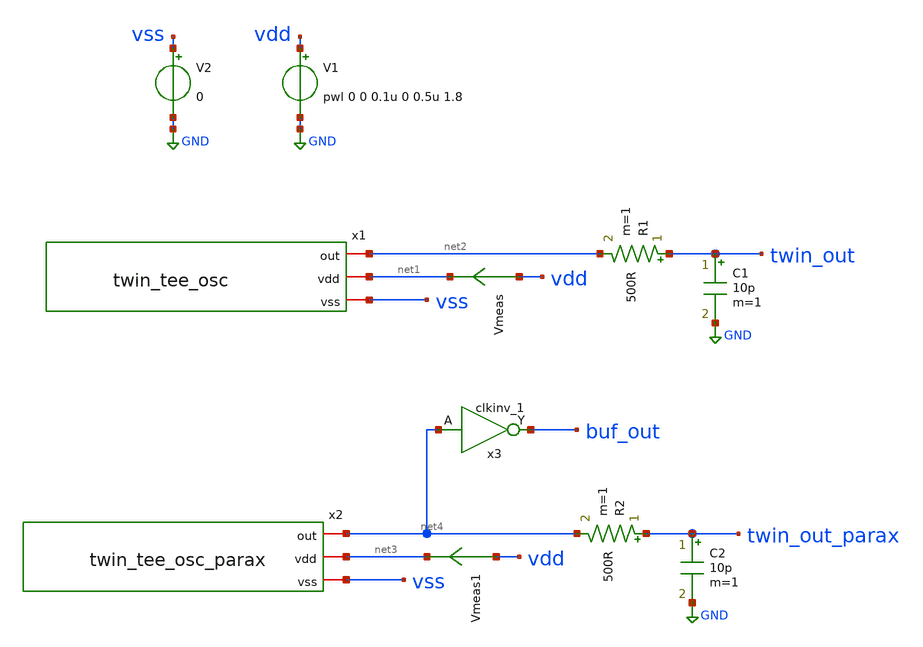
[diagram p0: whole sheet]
** sch_path: xschem/tb_twin_tee_osc.sch
**.subckt tb_twin_tee_osc
V1 vdd GND pwl 0 0 0.1u 0 0.5u 1.8
V2 vss GND 0
x1 net2 net1 vss twin_tee_osc
Vmeas vdd net1 0
R1 twin_out net2 500R m=1
C1 twin_out GND 10p m=1
x2 net4 net3 vss twin_tee_osc_parax
Vmeas1 vdd net3 0
R2 twin_out_parax net4 500R m=1
C2 twin_out_parax GND 10p m=1
x3 net4 vss vss vdd vdd buf_out sky130_fd_sc_hd__clkinv_1
**** begin user architecture code

** opencircuitdesign pdks install
.lib $::SKYWATER_MODELS/sky130.lib.spice tt_mm
.include $::SKYWATER_STDCELLS/sky130_fd_sc_hd.spice





*.option  METHOD = GEAR
*.param mc_mm_switch=0
.control
repeat 5

  tran 500p 10u uic
  write tb_twin_tee_osc.raw
  set appendwrite
  reset

end
.endc



**** end user architecture code
**.ends
.GLOBAL GND
.end
